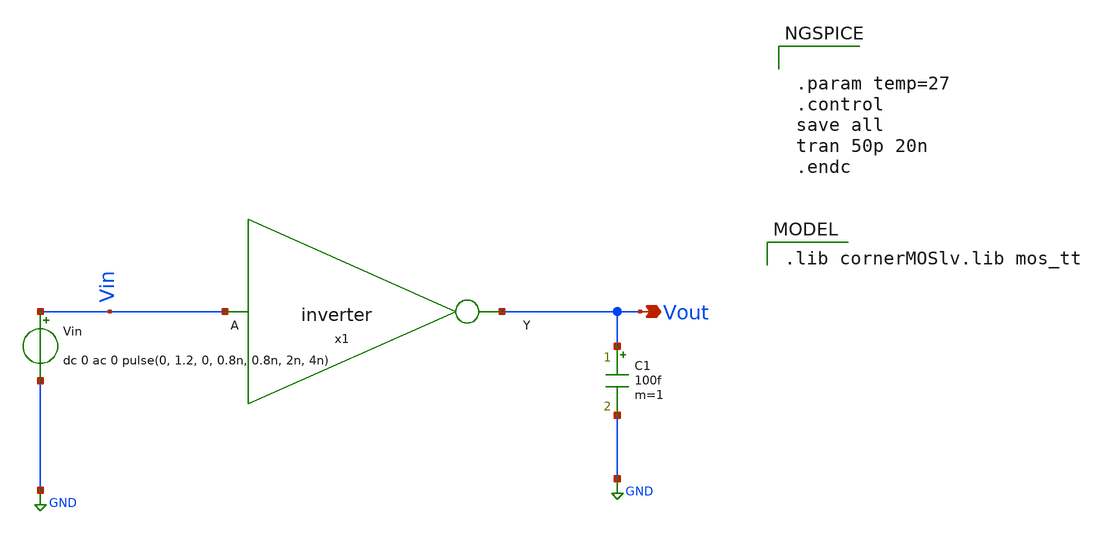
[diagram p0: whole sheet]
** sch_path: Team 1 Design/design_data/xschem/inverter/inverter_tb.sch
**.subckt inverter_tb Vout
*.opin Vout
x1 Vout Vin inverter
Vin Vin GND dc 0 ac 0 pulse(0, 1.2, 0, 0.8n, 0.8n, 2n, 4n)
C1 Vout GND 100f m=1
**** begin user architecture code
 .lib cornerMOSlv.lib mos_tt



.param temp=27
.control
save all
tran 50p 20n
.endc


**** end user architecture code
**.ends
.GLOBAL GND
.end
